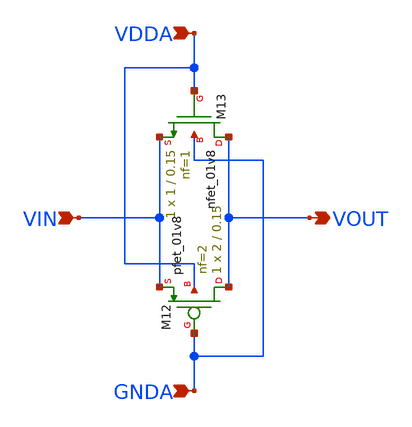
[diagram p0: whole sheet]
** sch_path: projects/pll/divider/xschem_ngspice/passgate.sch
**.subckt passgate VDDA GNDA VIN VOUT
*.ipin VDDA
*.ipin GNDA
*.ipin VIN
*.opin VOUT
XM12 VOUT GNDA VIN VDDA sky130_fd_pr__pfet_01v8 L=0.15 W=2 nf=2 ad='int((nf+1)/2) * W/nf * 0.29' as='int((nf+2)/2) * W/nf * 0.29'
+ pd='2*int((nf+1)/2) * (W/nf + 0.29)' ps='2*int((nf+2)/2) * (W/nf + 0.29)' nrd='0.29 / W' nrs='0.29 / W'
+ sa=0 sb=0 sd=0 mult=1 m=1
XM13 VOUT VDDA VIN GNDA sky130_fd_pr__nfet_01v8 L=0.15 W=1 nf=1 ad='int((nf+1)/2) * W/nf * 0.29' as='int((nf+2)/2) * W/nf * 0.29'
+ pd='2*int((nf+1)/2) * (W/nf + 0.29)' ps='2*int((nf+2)/2) * (W/nf + 0.29)' nrd='0.29 / W' nrs='0.29 / W'
+ sa=0 sb=0 sd=0 mult=1 m=1
**.ends
.end
